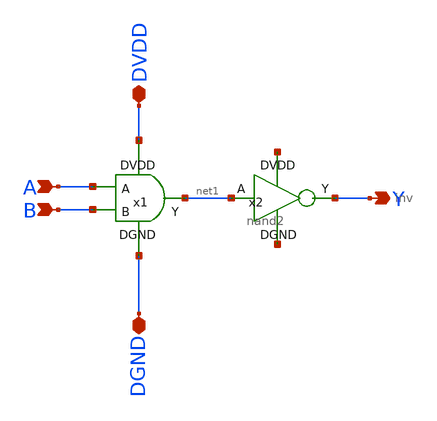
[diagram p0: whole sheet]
** sch_path: project/sch_sym_files/and.sch
**.subckt and A B Y DVDD DGND
*.ipin A
*.ipin B
*.opin Y
*.iopin DVDD
*.iopin DGND
x1 DVDD A B net1 DGND nand2
x2 net1 Y net2 net3 inv
**.ends

* expanding   symbol:  nand2.sym # of pins=5
** sym_path: project/sch_sym_files/nand2.sym
** sch_path: project/sch_sym_files/nand2.sch
.subckt nand2 DVDD A B Y DGND
*.opin Y
*.ipin A
*.iopin DVDD
*.iopin DGND
*.ipin B
XM2 Y A DVDD DVDD sky130_fd_pr__pfet_01v8 L=0.15 W=1.00 nf=1 ad='int((nf+1)/2) * W/nf * 0.29' as='int((nf+2)/2) * W/nf * 0.29'
+ pd='2*int((nf+1)/2) * (W/nf + 0.29)' ps='2*int((nf+2)/2) * (W/nf + 0.29)' nrd='0.29 / W' nrs='0.29 / W'
+ sa=0 sb=0 sd=0 mult=1 m=1
XM1 Y A net1 DGND sky130_fd_pr__nfet_01v8 L=0.15 W=0.65 nf=1 ad='int((nf+1)/2) * W/nf * 0.29' as='int((nf+2)/2) * W/nf * 0.29'
+ pd='2*int((nf+1)/2) * (W/nf + 0.29)' ps='2*int((nf+2)/2) * (W/nf + 0.29)' nrd='0.29 / W' nrs='0.29 / W'
+ sa=0 sb=0 sd=0 mult=1 m=1
XM3 net1 B DGND DGND sky130_fd_pr__nfet_01v8 L=0.15 W=0.65 nf=1 ad='int((nf+1)/2) * W/nf * 0.29' as='int((nf+2)/2) * W/nf * 0.29'
+ pd='2*int((nf+1)/2) * (W/nf + 0.29)' ps='2*int((nf+2)/2) * (W/nf + 0.29)' nrd='0.29 / W' nrs='0.29 / W'
+ sa=0 sb=0 sd=0 mult=1 m=1
XM7 Y B DVDD DVDD sky130_fd_pr__pfet_01v8 L=0.15 W=1.00 nf=1 ad='int((nf+1)/2) * W/nf * 0.29' as='int((nf+2)/2) * W/nf * 0.29'
+ pd='2*int((nf+1)/2) * (W/nf + 0.29)' ps='2*int((nf+2)/2) * (W/nf + 0.29)' nrd='0.29 / W' nrs='0.29 / W'
+ sa=0 sb=0 sd=0 mult=1 m=1
.ends


* expanding   symbol:  inv.sym # of pins=4
** sym_path: project/sch_sym_files/inv.sym
** sch_path: project/sch_sym_files/inv.sch
.subckt inv A Y DVDD DGND
*.opin Y
*.ipin A
*.iopin DVDD
*.iopin DGND
XM2 Y A DVDD DVDD sky130_fd_pr__pfet_01v8 L=0.15 W=1.00 nf=1 ad='int((nf+1)/2) * W/nf * 0.29' as='int((nf+2)/2) * W/nf * 0.29'
+ pd='2*int((nf+1)/2) * (W/nf + 0.29)' ps='2*int((nf+2)/2) * (W/nf + 0.29)' nrd='0.29 / W' nrs='0.29 / W'
+ sa=0 sb=0 sd=0 mult=1 m=1
XM1 Y A DGND DGND sky130_fd_pr__nfet_01v8 L=0.15 W=0.65 nf=1 ad='int((nf+1)/2) * W/nf * 0.29' as='int((nf+2)/2) * W/nf * 0.29'
+ pd='2*int((nf+1)/2) * (W/nf + 0.29)' ps='2*int((nf+2)/2) * (W/nf + 0.29)' nrd='0.29 / W' nrs='0.29 / W'
+ sa=0 sb=0 sd=0 mult=1 m=1
.ends

.end
